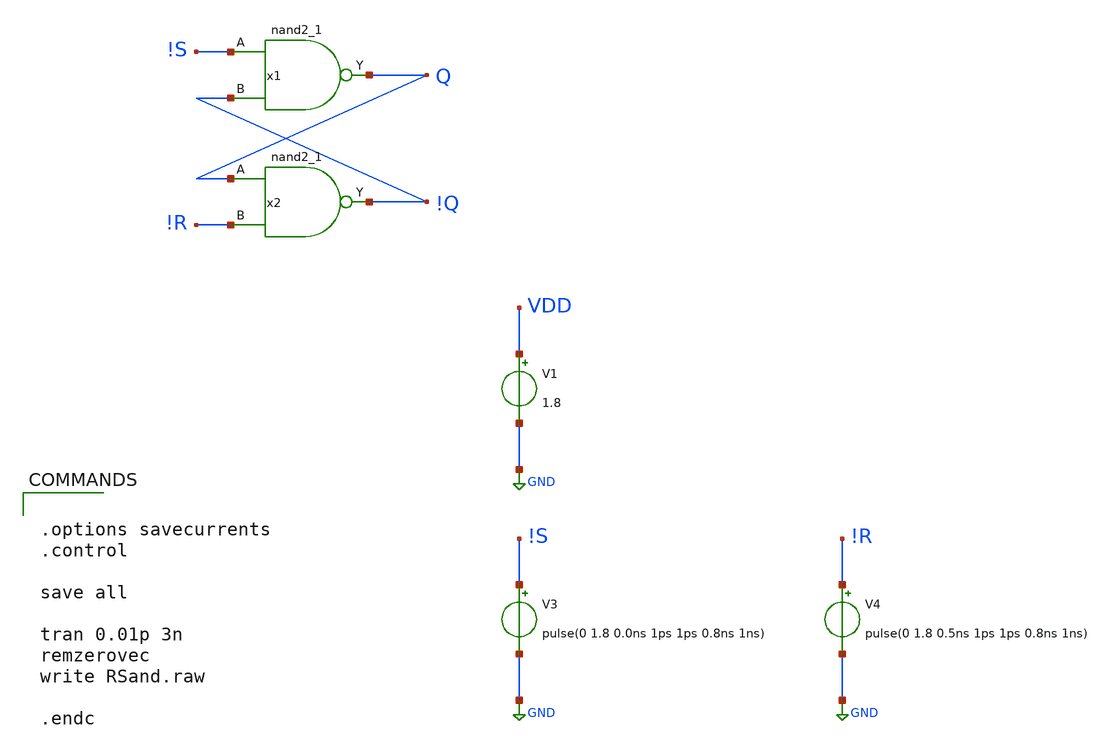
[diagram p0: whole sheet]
** sch_path: RSlatch/xschem/RSand.sch
.lib $::SKYWATER_MODELS/sky130.lib.spice tt
.include $::SKYWATER_STDCELLS/sky130_fd_sc_hd.spice

**.subckt RSand
V1 VDD GND 1.8
x1 !S !Q GND GND VDD VDD Q sky130_fd_sc_hd__nand2_1
x2 Q !R GND GND VDD VDD !Q sky130_fd_sc_hd__nand2_1
V4 !R GND pulse(0 1.8 0.5ns 1ps 1ps 0.8ns 1ns)
V3 !S GND pulse(0 1.8 0.0ns 1ps 1ps 0.8ns 1ns)
**** begin user architecture code


.options savecurrents
.control

save all

tran 0.01p 3n
remzerovec
write RSand.raw

.endc


**** end user architecture code
**.ends
.GLOBAL GND
.end
